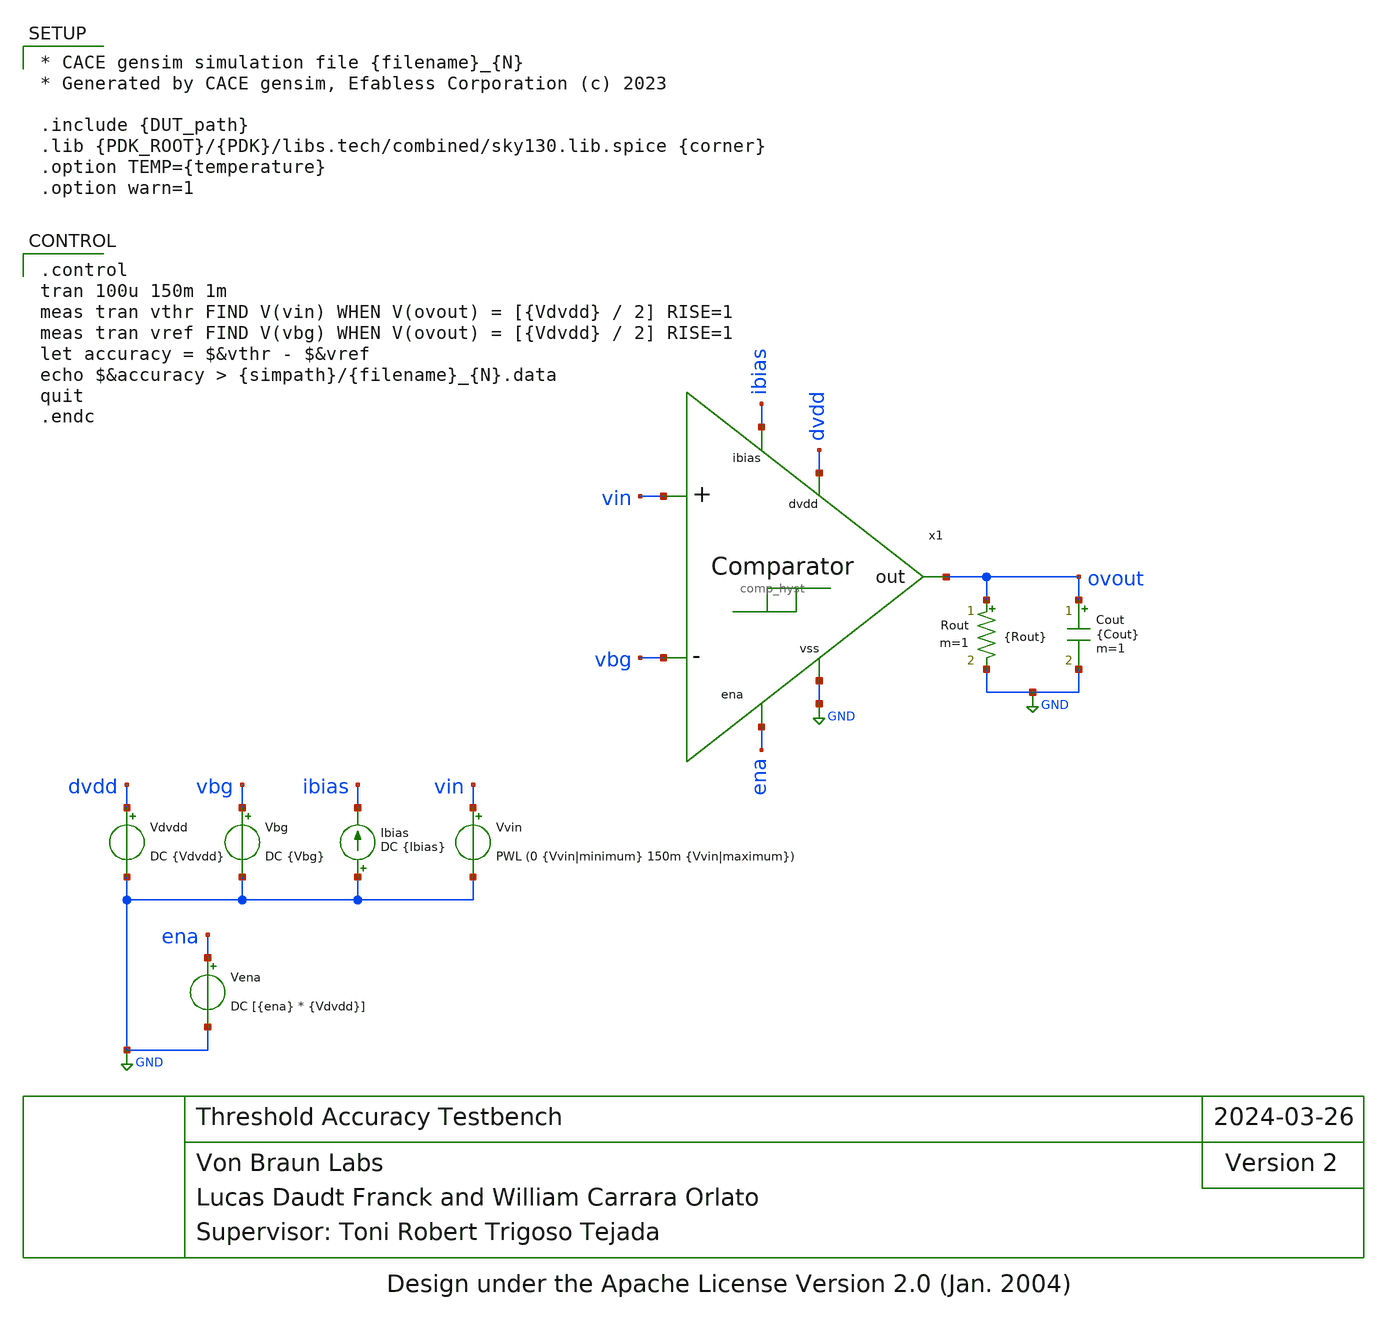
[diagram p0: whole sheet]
** sch_path: blocks/comp_hyst/cace/tb_vacc.sch
* Design under the Apache License Version 2.0 (Jan. 2004)
**.subckt tb_vacc
Vvin vin GND PWL (0 {Vvin|minimum} 150m {Vvin|maximum})
Vdvdd dvdd GND DC {Vdvdd}
Vbg vbg GND DC {Vbg}
Ibias GND ibias DC {Ibias}
Vena ena GND DC [{ena} * {Vdvdd}]
Cout ovout GND {Cout} m=1
Rout ovout GND {Rout} m=1
x1 dvdd ovout vbg vin ena ibias GND comp_hyst
**** begin user architecture code

* CACE gensim simulation file {filename}_{N}
* Generated by CACE gensim, Efabless Corporation (c) 2023

.include {DUT_path}
.lib {PDK_ROOT}/{PDK}/libs.tech/combined/sky130.lib.spice {corner}
.option TEMP={temperature}
.option warn=1



.control
tran 100u 150m 1m
meas tran vthr FIND V(vin) WHEN V(ovout) = [{Vdvdd} / 2] RISE=1
meas tran vref FIND V(vbg) WHEN V(ovout) = [{Vdvdd} / 2] RISE=1
let accuracy = $&vthr - $&vref
echo $&accuracy > {simpath}/{filename}_{N}.data
quit
.endc


**** end user architecture code
**.ends
.GLOBAL GND
.end
